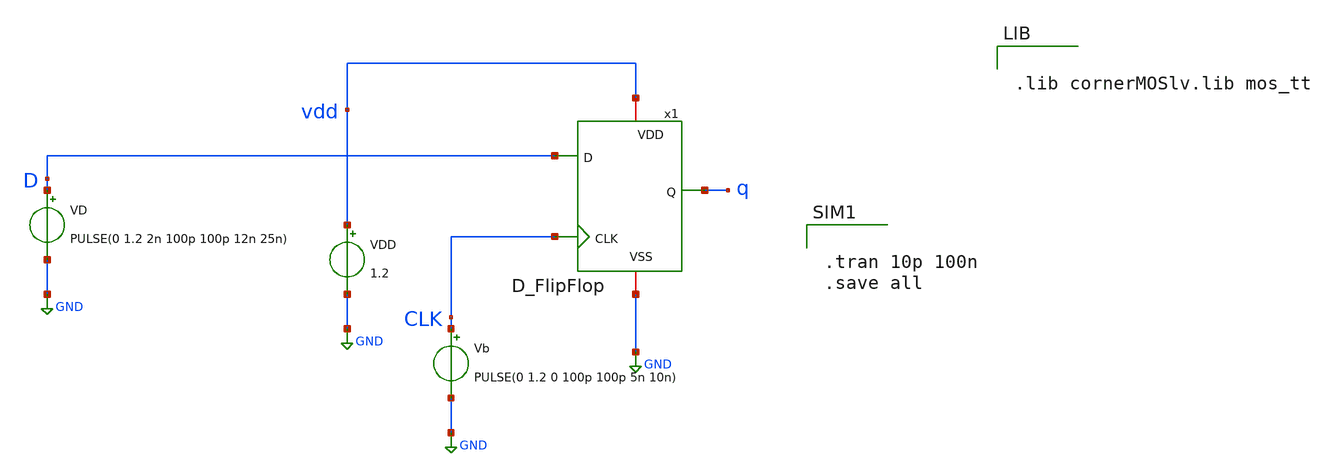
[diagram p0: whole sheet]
** sch_path: TestDFF.sch
**.subckt TestDFF
x1 D q CLK vdd GND D_FlipFlop
VD D GND PULSE(0 1.2 2n 100p 100p 12n 25n)
VDD vdd GND 1.2
Vb CLK GND PULSE(0 1.2 0 100p 100p 5n 10n)
**** begin user architecture code


.lib cornerMOSlv.lib mos_tt




.tran 10p 100n
.save all


**** end user architecture code
**.ends

* expanding   symbol:  /foss/designs/LogicGate/D_FlipFlop.sym # of pins=5
** sym_path: LogicGate/D_FlipFlop.sym
** sch_path: LogicGate/D_FlipFlop.sch
.subckt D_FlipFlop D Q CLK VDD VSS
*.ipin D
*.ipin CLK
*.opin Q
*.iopin VDD
*.iopin VSS
xTG1 VDD CLK QM1 D CLKB VSS Tranmission
xTG2 VDD CLKB QS1 QM2 CLK VSS Tranmission
xTG_fb1 VDD CLKB QM1 net1 CLK VSS Tranmission
xTG_fb2 VDD CLK QS1 net2 CLKB VSS Tranmission
x1 VDD QM1 QM2 VSS inverter
x2 VDD QM2 net1 VSS inverter
x3 VDD QS1 Q VSS inverter
x4 VDD Q net2 VSS inverter
x5 VDD QM1 QM2 VSS inverter
x6 VDD CLK CLKB VSS inverter
.ends


* expanding   symbol:  /foss/designs/LogicGate/Tranmission.sym # of pins=6
** sym_path: LogicGate/Tranmission.sym
** sch_path: LogicGate/Tranmission.sch
.subckt Tranmission VDD ENB OUT IN EN VSS
*.ipin IN
*.opin OUT
*.iopin VDD
*.iopin VSS
*.ipin EN
*.ipin ENB
XXM1 OUT ENB IN VDD sg13_lv_pmos w=0.15u l=0.13u ng=1 m=1 mm_ok=1
XXM2 OUT EN IN VSS sg13_lv_nmos w=0.15u l=0.13u ng=1 m=1 mm_ok=1
.ends


* expanding   symbol:  /foss/designs/BTDay6-Ex/inverter.sym # of pins=4
** sym_path: BTDay6-Ex/inverter.sym
** sch_path: BTDay6-Ex/inverter.sch
.subckt inverter VDD A Y VSS
*.ipin A
*.opin Y
*.iopin VDD
*.iopin VSS
XM1 Y A VSS VSS sg13_lv_nmos w=0.15u l=0.13u ng=1 m=1 mm_ok=1
XM2 Y A VDD VDD sg13_lv_pmos w=0.15u l=0.13u ng=1 m=1 mm_ok=1
.ends

.GLOBAL GND
.end
